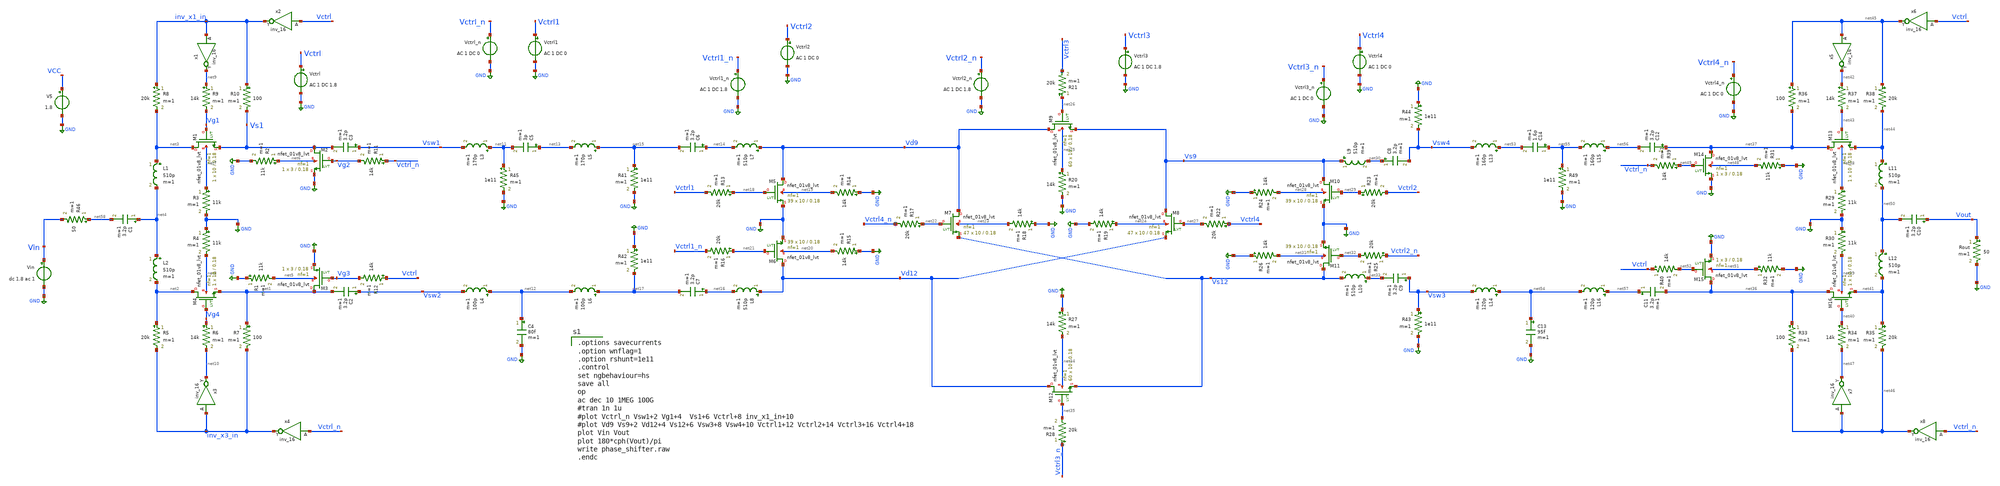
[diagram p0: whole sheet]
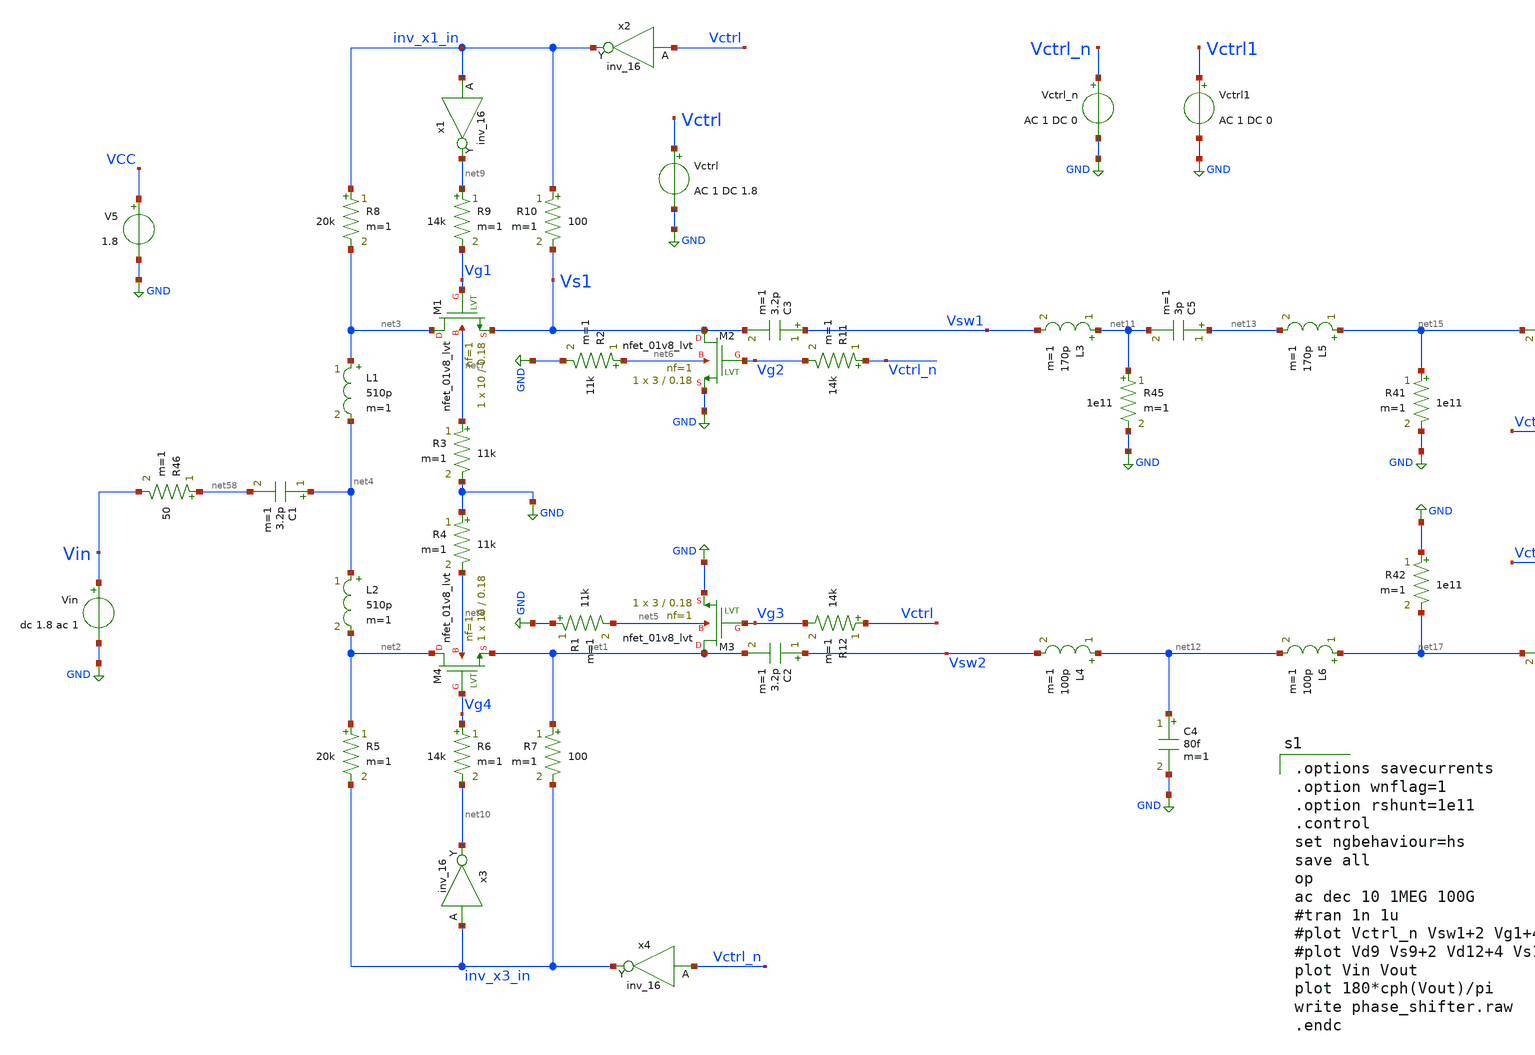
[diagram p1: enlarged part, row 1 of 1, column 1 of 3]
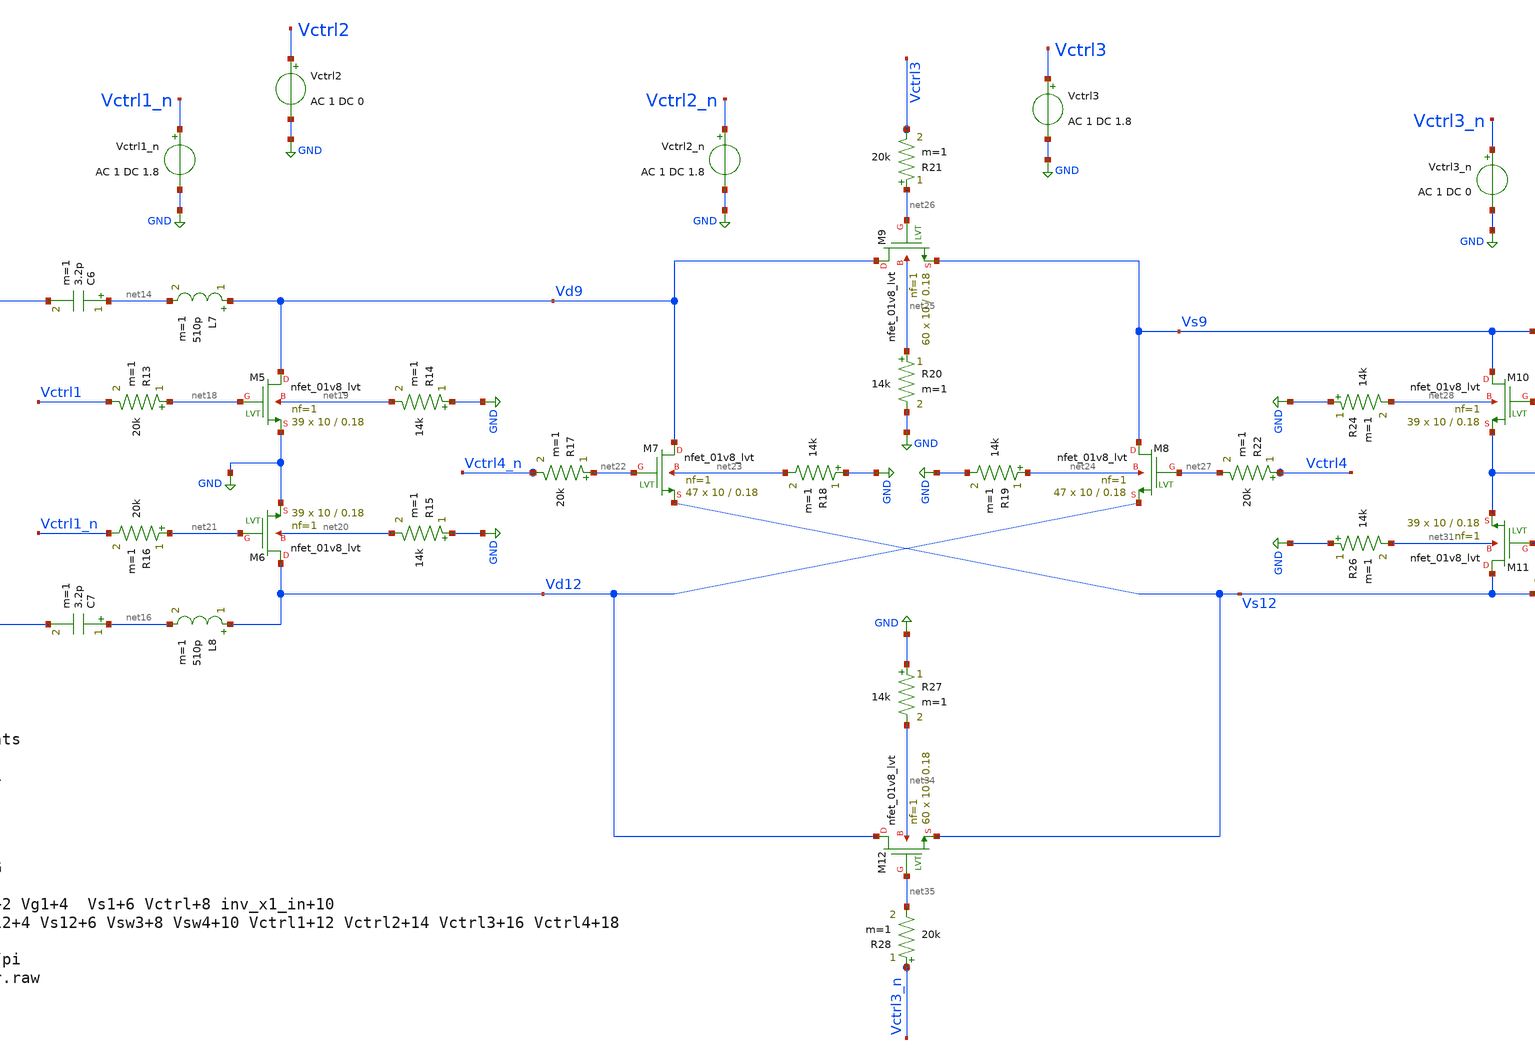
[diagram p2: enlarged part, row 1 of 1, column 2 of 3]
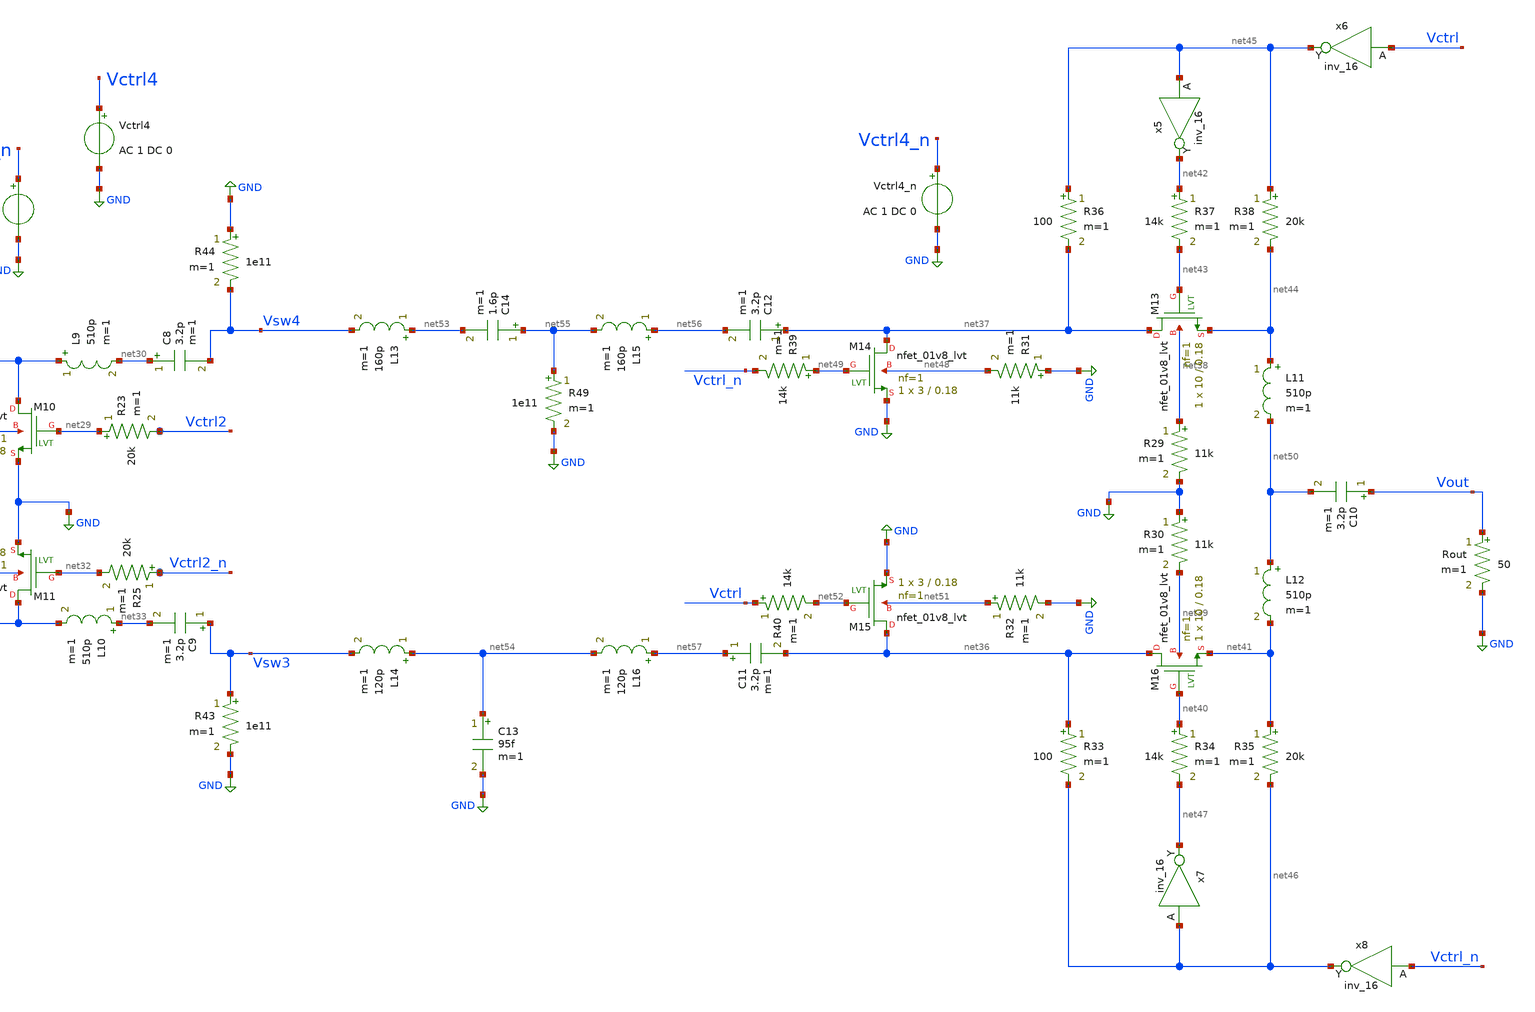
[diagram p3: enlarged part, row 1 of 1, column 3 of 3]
** sch_path: phase_shifter.sch
**.subckt phase_shifter
XM1 net3 Vg1 Vs1 net7 sky130_fd_pr__nfet_01v8_lvt L=0.18 W=10 nf=1 ad=0 as=0 pd=0 ps=0 nrd=0 nrs=0
+ sa=0 sb=0 sd=0 mult=1 m=1
XM2 Vs1 Vg2 GND net6 sky130_fd_pr__nfet_01v8_lvt L=0.18 W=3 nf=1 ad=0 as=0 pd=0 ps=0 nrd=0 nrs=0
+ sa=0 sb=0 sd=0 mult=1 m=1
XM3 net1 Vg3 GND net5 sky130_fd_pr__nfet_01v8_lvt L=0.18 W=3 nf=1 ad=0 as=0 pd=0 ps=0 nrd=0 nrs=0
+ sa=0 sb=0 sd=0 mult=1 m=1
XM4 net2 Vg4 net1 net8 sky130_fd_pr__nfet_01v8_lvt L=0.18 W=10 nf=1 ad=0 as=0 pd=0 ps=0 nrd=0 nrs=0
+ sa=0 sb=0 sd=0 mult=1 m=1
L1 net3 net4 510p m=1
L2 net4 net2 510p m=1
R3 net7 GND 11k m=1
R4 GND net8 11k m=1
R2 net6 GND 11k m=1
R1 GND net5 11k m=1
R5 net2 inv_x3_in 20k m=1
R6 Vg4 net10 14k m=1
R7 net1 inv_x3_in 100 m=1
R8 inv_x1_in net3 20k m=1
R9 net9 Vg1 14k m=1
R10 inv_x1_in Vs1 100 m=1
x1 inv_x1_in GND GND VCC VCC net9 sky130_fd_sc_hd__inv_16
x2 Vctrl GND GND VCC VCC inv_x1_in sky130_fd_sc_hd__inv_16
x3 inv_x3_in GND GND VCC VCC net10 sky130_fd_sc_hd__inv_16
x4 Vctrl_n GND GND VCC VCC inv_x3_in sky130_fd_sc_hd__inv_16
R11 Vctrl_n Vg2 14k m=1
R12 Vctrl Vg3 14k m=1
C1 net4 net58 3.2p m=1
C2 Vsw2 net1 3.2p m=1
C3 Vsw1 Vs1 3.2p m=1
Vctrl Vctrl GND AC 1 DC 1.8
Vctrl_n Vctrl_n GND AC 1 DC 0
L3 net11 Vsw1 170p m=1
L4 net12 Vsw2 100p m=1
C4 net12 GND 80f m=1
C5 net13 net11 3p m=1
L5 net15 net13 170p m=1
L6 net17 net12 100p m=1
C6 net14 net15 3.2p m=1
L7 Vd9 net14 510p m=1
C7 net16 net17 3.2p m=1
L8 Vd12 net16 510p m=1
XM5 Vd9 net18 GND net19 sky130_fd_pr__nfet_01v8_lvt L=0.18 W=10 nf=1 ad=0 as=0 pd=0 ps=0 nrd=0 nrs=0
+ sa=0 sb=0 sd=0 mult=39 m=39
R13 net18 Vctrl1 20k m=1
R14 GND net19 14k m=1
XM6 Vd12 net21 GND net20 sky130_fd_pr__nfet_01v8_lvt L=0.18 W=10 nf=1 ad=0 as=0 pd=0 ps=0 nrd=0
+ nrs=0 sa=0 sb=0 sd=0 mult=39 m=39
R15 GND net20 14k m=1
R16 net21 Vctrl1_n 20k m=1
XM7 Vd9 net22 Vs12 net23 sky130_fd_pr__nfet_01v8_lvt L=0.18 W=10 nf=1 ad=0 as=0 pd=0 ps=0 nrd=0
+ nrs=0 sa=0 sb=0 sd=0 mult=47 m=47
R17 net22 Vctrl4_n 20k m=1
R18 GND net23 14k m=1
R19 net24 GND 14k m=1
XM8 Vs9 net27 Vd12 net24 sky130_fd_pr__nfet_01v8_lvt L=0.18 W=10 nf=1 ad=0 as=0 pd=0 ps=0 nrd=0
+ nrs=0 sa=0 sb=0 sd=0 mult=47 m=47
XM9 Vd9 net26 Vs9 net25 sky130_fd_pr__nfet_01v8_lvt L=0.18 W=10 nf=1 ad=0 as=0 pd=0 ps=0 nrd=0 nrs=0
+ sa=0 sb=0 sd=0 mult=60 m=60
R20 net25 GND 14k m=1
R21 net26 Vctrl3 20k m=1
R22 Vctrl4 net27 20k m=1
C8 net30 Vsw4 3.2p m=1
L9 Vs9 net30 510p m=1
XM10 Vs9 net29 GND net28 sky130_fd_pr__nfet_01v8_lvt L=0.18 W=10 nf=1 ad=0 as=0 pd=0 ps=0 nrd=0
+ nrs=0 sa=0 sb=0 sd=0 mult=39 m=39
R23 net29 Vctrl2 20k m=1
R24 GND net28 14k m=1
XM11 Vs12 net32 GND net31 sky130_fd_pr__nfet_01v8_lvt L=0.18 W=10 nf=1 ad=0 as=0 pd=0 ps=0 nrd=0
+ nrs=0 sa=0 sb=0 sd=0 mult=39 m=39
R25 Vctrl2_n net32 20k m=1
R26 GND net31 14k m=1
C9 Vsw3 net33 3.2p m=1
L10 net33 Vs12 510p m=1
XM12 Vd12 net35 Vs12 net34 sky130_fd_pr__nfet_01v8_lvt L=0.18 W=10 nf=1 ad=0 as=0 pd=0 ps=0 nrd=0
+ nrs=0 sa=0 sb=0 sd=0 mult=60 m=60
R27 GND net34 14k m=1
R28 Vctrl3_n net35 20k m=1
Vctrl1 Vctrl1 GND AC 1 DC 0
Vctrl1_n Vctrl1_n GND AC 1 DC 1.8
Vctrl2 Vctrl2 GND AC 1 DC 0
Vctrl2_n Vctrl2_n GND AC 1 DC 1.8
Vctrl3 Vctrl3 GND AC 1 DC 1.8
Vctrl3_n Vctrl3_n GND AC 1 DC 0
Vctrl4 Vctrl4 GND AC 1 DC 0
Vctrl4_n Vctrl4_n GND AC 1 DC 0
XM13 net37 net43 net44 net38 sky130_fd_pr__nfet_01v8_lvt L=0.18 W=10 nf=1 ad=0 as=0 pd=0 ps=0 nrd=0
+ nrs=0 sa=0 sb=0 sd=0 mult=1 m=1
XM14 net37 net49 GND net48 sky130_fd_pr__nfet_01v8_lvt L=0.18 W=3 nf=1 ad=0 as=0 pd=0 ps=0 nrd=0
+ nrs=0 sa=0 sb=0 sd=0 mult=1 m=1
XM16 net36 net40 net41 net39 sky130_fd_pr__nfet_01v8_lvt L=0.18 W=10 nf=1 ad=0 as=0 pd=0 ps=0 nrd=0
+ nrs=0 sa=0 sb=0 sd=0 mult=1 m=1
L11 net44 net50 510p m=1
L12 net50 net41 510p m=1
R29 net38 GND 11k m=1
R30 GND net39 11k m=1
R31 GND net48 11k m=1
R33 net36 net46 100 m=1
R34 net40 net47 14k m=1
R35 net41 net46 20k m=1
R36 net45 net37 100 m=1
R37 net42 net43 14k m=1
R38 net45 net44 20k m=1
x5 net45 GND GND VCC VCC net42 sky130_fd_sc_hd__inv_16
x6 Vctrl GND GND VCC VCC net45 sky130_fd_sc_hd__inv_16
x7 net46 GND GND VCC VCC net47 sky130_fd_sc_hd__inv_16
x8 Vctrl_n GND GND VCC VCC net46 sky130_fd_sc_hd__inv_16
R39 net49 Vctrl_n 14k m=1
C10 Vout net50 3.2p m=1
C12 net37 net56 3.2p m=1
XM15 net36 net52 GND net51 sky130_fd_pr__nfet_01v8_lvt L=0.18 W=3 nf=1 ad=0 as=0 pd=0 ps=0 nrd=0
+ nrs=0 sa=0 sb=0 sd=0 mult=1 m=1
R32 net51 GND 11k m=1
R40 Vctrl net52 14k m=1
C11 net57 net36 3.2p m=1
Vin Vin GND dc 1.8 ac 1
Rout Vout GND 50 m=1
V5 VCC GND 1.8
R41 net15 GND 1e11 m=1
R42 GND net17 1e11 m=1
R43 Vsw3 GND 1e11 m=1
R44 GND Vsw4 1e11 m=1
R45 net11 GND 1e11 m=1
L13 net53 Vsw4 160p m=1
L14 net54 Vsw3 120p m=1
C13 net54 GND 95f m=1
C14 net55 net53 1.6p m=1
L15 net56 net55 160p m=1
L16 net57 net54 120p m=1
R49 net55 GND 1e11 m=1
R46 net58 Vin 50 m=1
**** begin user architecture code

.options savecurrents
.option wnflag=1
.option rshunt=1e11
.control
set ngbehaviour=hs
save all
op
ac dec 10 1MEG 100G
#tran 1n 1u
#plot Vctrl_n Vsw1+2 Vg1+4  Vs1+6 Vctrl+8 inv_x1_in+10
#plot Vd9 Vs9+2 Vd12+4 Vs12+6 Vsw3+8 Vsw4+10 Vctrl1+12 Vctrl2+14 Vctrl3+16 Vctrl4+18
plot Vin Vout
plot 180*cph(Vout)/pi
write phase_shifter.raw
.endc


[sky130_models]


.include $::SKYWATER_MODELS/cells/nfet_01v8/sky130_fd_pr__nfet_01v8__tt.corner.spice
.include $::SKYWATER_MODELS/cells/nfet_01v8_lvt/sky130_fd_pr__nfet_01v8_lvt__tt.corner.spice
.include $::SKYWATER_MODELS/cells/pfet_01v8/sky130_fd_pr__pfet_01v8__tt.corner.spice
.include $::SKYWATER_MODELS/cells/nfet_03v3_nvt/sky130_fd_pr__nfet_03v3_nvt__tt.corner.spice
.include $::SKYWATER_MODELS/cells/nfet_05v0_nvt/sky130_fd_pr__nfet_05v0_nvt__tt.corner.spice
.include $::SKYWATER_MODELS/cells/esd_nfet_01v8/sky130_fd_pr__esd_nfet_01v8__tt.corner.spice
.include $::SKYWATER_MODELS/cells/pfet_01v8_lvt/sky130_fd_pr__pfet_01v8_lvt__tt.corner.spice
.include $::SKYWATER_MODELS/cells/pfet_01v8_hvt/sky130_fd_pr__pfet_01v8_hvt__tt.corner.spice
.include $::SKYWATER_MODELS/cells/esd_pfet_g5v0d10v5/sky130_fd_pr__esd_pfet_g5v0d10v5__tt.corner.spice
.include $::SKYWATER_MODELS/cells/pfet_g5v0d10v5/sky130_fd_pr__pfet_g5v0d10v5__tt.corner.spice
.include $::SKYWATER_MODELS/cells/pfet_g5v0d16v0/sky130_fd_pr__pfet_g5v0d16v0__tt.corner.spice
.include $::SKYWATER_MODELS/cells/nfet_g5v0d10v5/sky130_fd_pr__nfet_g5v0d10v5__tt.corner.spice
.include $::SKYWATER_MODELS/cells/nfet_g5v0d16v0/sky130_fd_pr__nfet_g5v0d16v0__tt_discrete.corner.spice
.include $::SKYWATER_MODELS/cells/esd_nfet_g5v0d10v5/sky130_fd_pr__esd_nfet_g5v0d10v5__tt.corner.spice
.include $::SKYWATER_MODELS/models/corners/tt/nonfet.spice
* Mismatch parameters
.include $::SKYWATER_MODELS/cells/nfet_01v8/sky130_fd_pr__nfet_01v8__mismatch.corner.spice
.include $::SKYWATER_MODELS/cells/pfet_01v8/sky130_fd_pr__pfet_01v8__mismatch.corner.spice
.include $::SKYWATER_MODELS/cells/nfet_01v8_lvt/sky130_fd_pr__nfet_01v8_lvt__mismatch.corner.spice
.include $::SKYWATER_MODELS/cells/pfet_01v8_lvt/sky130_fd_pr__pfet_01v8_lvt__mismatch.corner.spice
.include $::SKYWATER_MODELS/cells/pfet_01v8_hvt/sky130_fd_pr__pfet_01v8_hvt__mismatch.corner.spice
.include $::SKYWATER_MODELS/cells/nfet_g5v0d10v5/sky130_fd_pr__nfet_g5v0d10v5__mismatch.corner.spice
.include $::SKYWATER_MODELS/cells/pfet_g5v0d10v5/sky130_fd_pr__pfet_g5v0d10v5__mismatch.corner.spice
.include $::SKYWATER_MODELS/cells/nfet_05v0_nvt/sky130_fd_pr__nfet_05v0_nvt__mismatch.corner.spice
.include $::SKYWATER_MODELS/cells/nfet_03v3_nvt/sky130_fd_pr__nfet_03v3_nvt__mismatch.corner.spice
* Resistor$::SKYWATER_MODELS/Capacitor
.include $::SKYWATER_MODELS/models/r+c/res_typical__cap_typical.spice
.include $::SKYWATER_MODELS/models/r+c/res_typical__cap_typical__lin.spice
* Special cells
.include $::SKYWATER_MODELS/models/corners/tt/specialized_cells.spice
* All models
.include $::SKYWATER_MODELS/models/all.spice
* Corner
.include $::SKYWATER_MODELS/models/corners/tt/rf.spice

**** end user architecture code
**.ends
.GLOBAL GND
.end
